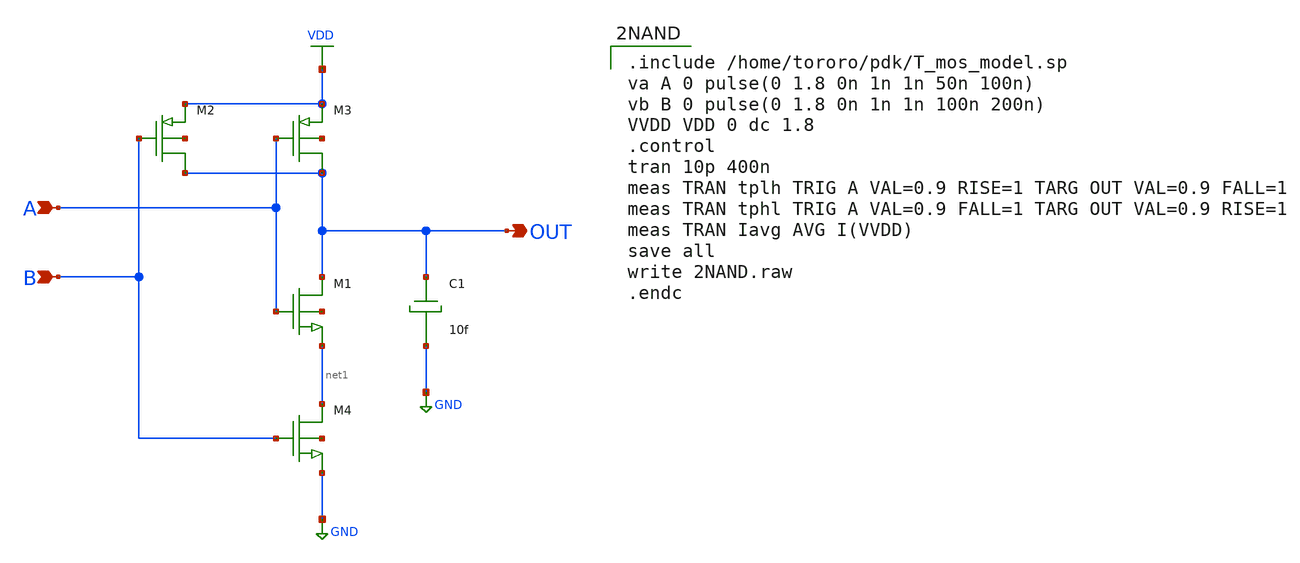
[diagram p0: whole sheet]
** sch_path: task1/2NAND.sch
**.subckt 2NAND OUT B A
*.opin OUT
*.ipin B
*.ipin A
M1 OUT A net1 net2 nch w=7.0u l=0.35u as=0 ps=0 ad=0 pd=0 m=1
M2 OUT B VDD net3 pch w=9.7u l=0.35u as=0 ps=0 ad=0 pd=0 m=1
M3 OUT A VDD net4 pch w=9.7u l=0.35u as=0 ps=0 ad=0 pd=0 m=1
M4 net1 B GND net5 nch w=7.0u l=0.35u as=0 ps=0 ad=0 pd=0 m=1
C1 OUT GND 10f m=1
**** begin user architecture code

.include /home/tororo/pdk/T_mos_model.sp
va A 0 pulse(0 1.8 0n 1n 1n 50n 100n)
vb B 0 pulse(0 1.8 0n 1n 1n 100n 200n)
VVDD VDD 0 dc 1.8
.control
tran 10p 400n
meas TRAN tplh TRIG A VAL=0.9 RISE=1 TARG OUT VAL=0.9 FALL=1
meas TRAN tphl TRIG A VAL=0.9 FALL=1 TARG OUT VAL=0.9 RISE=1
meas TRAN Iavg AVG I(VVDD)
save all
write 2NAND.raw
.endc

**** end user architecture code
**.ends
.GLOBAL VDD
.GLOBAL GND
.end
